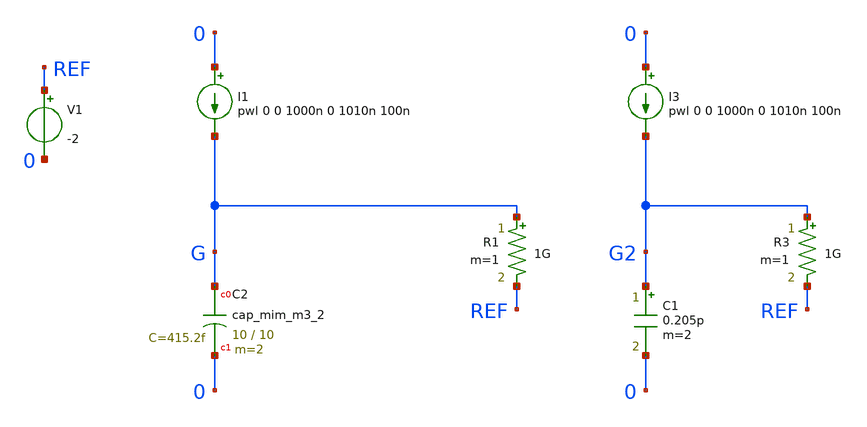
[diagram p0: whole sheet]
** sch_path: sky130A/xschem_libs/sky130_tests_ase/test_mim_cap/schematic/test_mim_cap.sch
* Copyright 2021 Stefan Frederik Schippers
* Licensed under the Apache License, Version 2.0 (the "License");
* you may not use this file except in compliance with the License.
* You may obtain a copy of the License at
* https://www.apache.org/licenses/LICENSE-2.0
* Unless required by applicable law or agreed to in writing, software
* distributed under the License is distributed on an "AS IS" BASIS,
* WITHOUT WARRANTIES OR CONDITIONS OF ANY KIND, either express or implied.
* See the License for the specific language governing permissions and
* limitations under the License.
**.subckt test_mim_cap
I1 0 G pwl 0 0 1000n 0 1010n 100n
R1 G REF 1G m=1
I3 0 G2 pwl 0 0 1000n 0 1010n 100n
R3 G2 REF 1G m=1
C1 G2 0 0.205p m=2
V1 REF 0 -2
XC2 G 0 sky130_fd_pr__cap_mim_m3_2 W=10 L=10 MF=2 m=2
**.ends
.end
